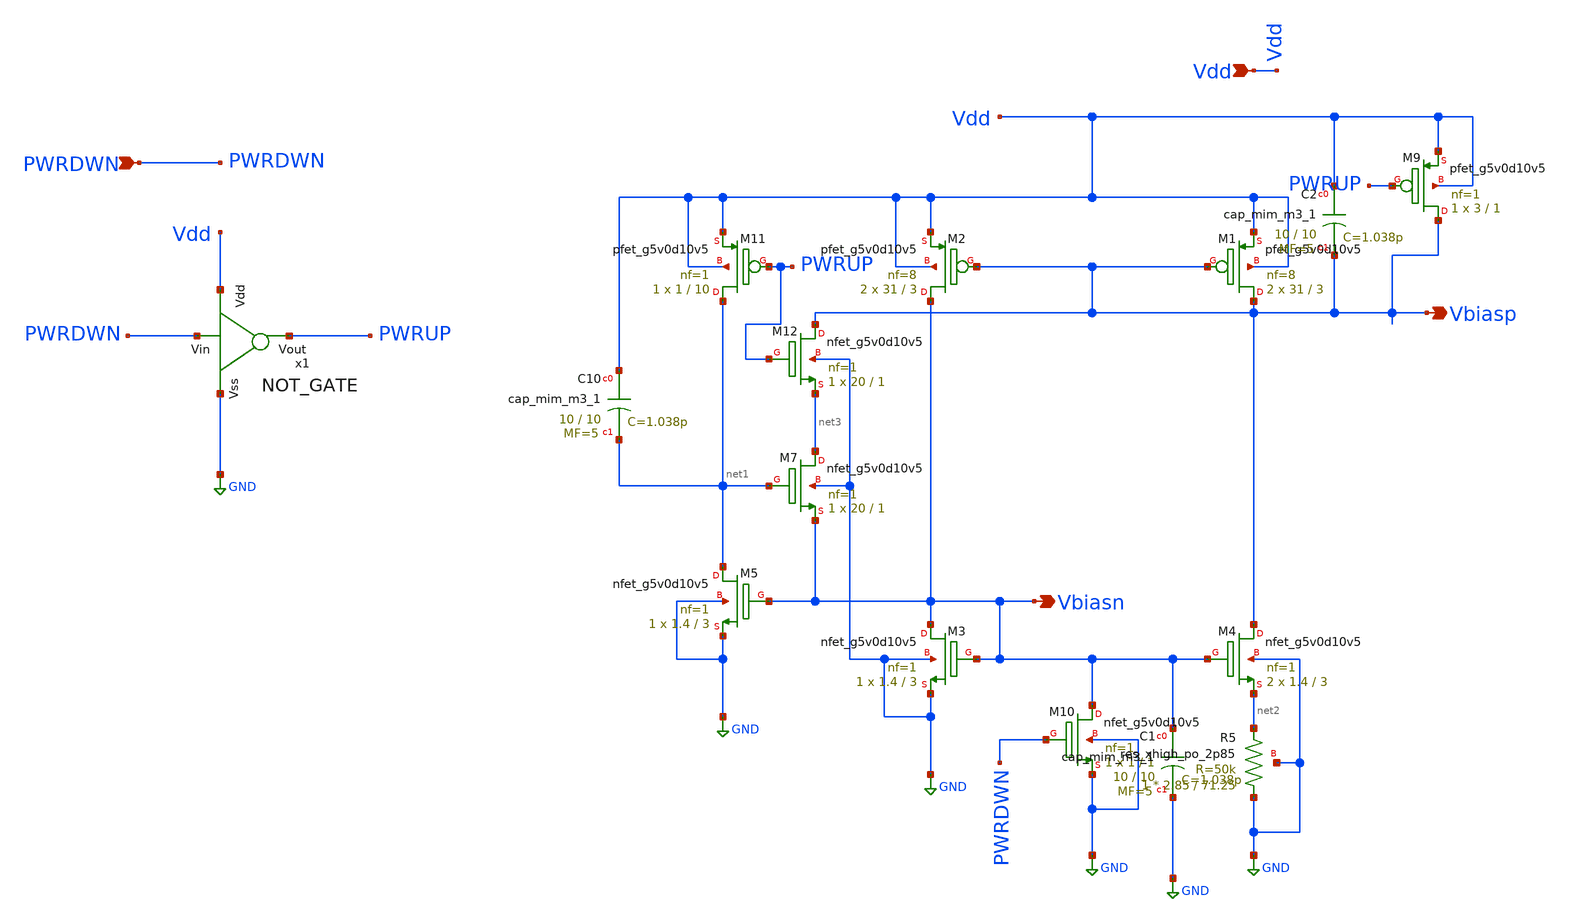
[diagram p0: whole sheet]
** sch_path: xschem/BMR.sch
**.subckt BMR Vdd Vbiasn Vbiasp PWRDWN
*.ipin Vdd
*.opin Vbiasn
*.opin Vbiasp
*.ipin PWRDWN
XM3 Vbiasn Vbiasn GND GND sky130_fd_pr__nfet_g5v0d10v5 L=3 W=1.4 nf=1 ad='int((1 + 1)/2) * 1.4 / 1 * 0.29'
+ as='int((1 + 2)/2) * 1.4 / 1 * 0.29' pd='2*int((1 + 1)/2) * (1.4 / 1 + 0.29)' ps='2*int((1 + 2)/2) * (1.4 / 1 + 0.29)'
+ nrd='0.29 / 1.4 ' nrs='0.29 / 1.4 ' sa=0 sb=0 sd=0 mult=1 m=1
XM1 Vbiasp Vbiasp Vdd Vdd sky130_fd_pr__pfet_g5v0d10v5 L=3 W=31 nf=8 ad='int((8 + 1)/2) * 31 / 8 * 0.29'
+ as='int((8 + 2)/2) * 31 / 8 * 0.29' pd='2*int((8 + 1)/2) * (31 / 8 + 0.29)' ps='2*int((8 + 2)/2) * (31 / 8 + 0.29)'
+ nrd='0.29 / 31 ' nrs='0.29 / 31 ' sa=0 sb=0 sd=0 mult=2 m=2
XM2 Vbiasn Vbiasp Vdd Vdd sky130_fd_pr__pfet_g5v0d10v5 L=3 W=31 nf=8 ad='int((8 + 1)/2) * 31 / 8 * 0.29'
+ as='int((8 + 2)/2) * 31 / 8 * 0.29' pd='2*int((8 + 1)/2) * (31 / 8 + 0.29)' ps='2*int((8 + 2)/2) * (31 / 8 + 0.29)'
+ nrd='0.29 / 31 ' nrs='0.29 / 31 ' sa=0 sb=0 sd=0 mult=2 m=2
XM11 net1 PWRUP Vdd Vdd sky130_fd_pr__pfet_g5v0d10v5 L=10 W=1 nf=1 ad='int((1 + 1)/2) * 1 / 1 * 0.29'
+ as='int((1 + 2)/2) * 1 / 1 * 0.29' pd='2*int((1 + 1)/2) * (1 / 1 + 0.29)' ps='2*int((1 + 2)/2) * (1 / 1 + 0.29)'
+ nrd='0.29 / 1 ' nrs='0.29 / 1 ' sa=0 sb=0 sd=0 mult=1 m=1
XM4 Vbiasp Vbiasn net2 GND sky130_fd_pr__nfet_g5v0d10v5 L=3 W=1.4 nf=1 ad='int((1 + 1)/2) * 1.4 / 1 * 0.29'
+ as='int((1 + 2)/2) * 1.4 / 1 * 0.29' pd='2*int((1 + 1)/2) * (1.4 / 1 + 0.29)' ps='2*int((1 + 2)/2) * (1.4 / 1 + 0.29)'
+ nrd='0.29 / 1.4 ' nrs='0.29 / 1.4 ' sa=0 sb=0 sd=0 mult=2 m=2
XM5 net1 Vbiasn GND GND sky130_fd_pr__nfet_g5v0d10v5 L=3 W=1.4 nf=1 ad='int((1 + 1)/2) * 1.4 / 1 * 0.29'
+ as='int((1 + 2)/2) * 1.4 / 1 * 0.29' pd='2*int((1 + 1)/2) * (1.4 / 1 + 0.29)' ps='2*int((1 + 2)/2) * (1.4 / 1 + 0.29)'
+ nrd='0.29 / 1.4 ' nrs='0.29 / 1.4 ' sa=0 sb=0 sd=0 mult=1 m=1
XM7 net3 net1 Vbiasn GND sky130_fd_pr__nfet_g5v0d10v5 L=1 W=20 nf=1 ad='int((1 + 1)/2) * 20 / 1 * 0.29'
+ as='int((1 + 2)/2) * 20 / 1 * 0.29' pd='2*int((1 + 1)/2) * (20 / 1 + 0.29)' ps='2*int((1 + 2)/2) * (20 / 1 + 0.29)'
+ nrd='0.29 / 20 ' nrs='0.29 / 20 ' sa=0 sb=0 sd=0 mult=1 m=1
x1 Vdd PWRUP PWRDWN GND NOT_GATE
XM12 Vbiasp PWRUP net3 GND sky130_fd_pr__nfet_g5v0d10v5 L=1 W=20 nf=1 ad='int((1 + 1)/2) * 20 / 1 * 0.29'
+ as='int((1 + 2)/2) * 20 / 1 * 0.29' pd='2*int((1 + 1)/2) * (20 / 1 + 0.29)' ps='2*int((1 + 2)/2) * (20 / 1 + 0.29)'
+ nrd='0.29 / 20 ' nrs='0.29 / 20 ' sa=0 sb=0 sd=0 mult=1 m=1
XM9 Vbiasp PWRUP Vdd Vdd sky130_fd_pr__pfet_g5v0d10v5 L=1 W=3 nf=1 ad='int((1 + 1)/2) * 3 / 1 * 0.29'
+ as='int((1 + 2)/2) * 3 / 1 * 0.29' pd='2*int((1 + 1)/2) * (3 / 1 + 0.29)' ps='2*int((1 + 2)/2) * (3 / 1 + 0.29)'
+ nrd='0.29 / 3 ' nrs='0.29 / 3 ' sa=0 sb=0 sd=0 mult=1 m=1
XM10 Vbiasn PWRDWN GND GND sky130_fd_pr__nfet_g5v0d10v5 L=1 W=1 nf=1 ad='int((1 + 1)/2) * 1 / 1 * 0.29'
+ as='int((1 + 2)/2) * 1 / 1 * 0.29' pd='2*int((1 + 1)/2) * (1 / 1 + 0.29)' ps='2*int((1 + 2)/2) * (1 / 1 + 0.29)'
+ nrd='0.29 / 1 ' nrs='0.29 / 1 ' sa=0 sb=0 sd=0 mult=1 m=1
XR5 GND net2 GND sky130_fd_pr__res_xhigh_po_2p85 L=71.25 mult=1 m=1
XC10 Vdd net1 sky130_fd_pr__cap_mim_m3_1 W=10 L=10 MF=5 m=5
XC2 Vdd Vbiasp sky130_fd_pr__cap_mim_m3_1 W=10 L=10 MF=5 m=5
XC1 Vbiasn GND sky130_fd_pr__cap_mim_m3_1 W=10 L=10 MF=5 m=5
**.ends

* expanding   symbol:  NOT_GATE.sym # of pins=4
** sym_path: xschem/NOT_GATE.sym
** sch_path: xschem/NOT_GATE.sch
.subckt NOT_GATE Vdd Vout Vin Vss
*.opin Vout
*.ipin Vdd
*.ipin Vss
*.ipin Vin
XM1 Vout Vin Vss Vss sky130_fd_pr__nfet_g5v0d10v5 L=1 W=1 nf=1 ad='int((1 + 1)/2) * 1 / 1 * 0.29' as='int((1 + 2)/2) * 1 / 1 * 0.29'
+ pd='2*int((1 + 1)/2) * (1 / 1 + 0.29)' ps='2*int((1 + 2)/2) * (1 / 1 + 0.29)' nrd='0.29 / 1 ' nrs='0.29 / 1 '
+ sa=0 sb=0 sd=0 mult=1 m=1
XM2 Vout Vin Vdd Vdd sky130_fd_pr__pfet_g5v0d10v5 L=1 W=3 nf=1 ad='int((1 + 1)/2) * 3 / 1 * 0.29' as='int((1 + 2)/2) * 3 / 1 * 0.29'
+ pd='2*int((1 + 1)/2) * (3 / 1 + 0.29)' ps='2*int((1 + 2)/2) * (3 / 1 + 0.29)' nrd='0.29 / 3 ' nrs='0.29 / 3 '
+ sa=0 sb=0 sd=0 mult=1 m=1
.ends

.GLOBAL GND
.end
